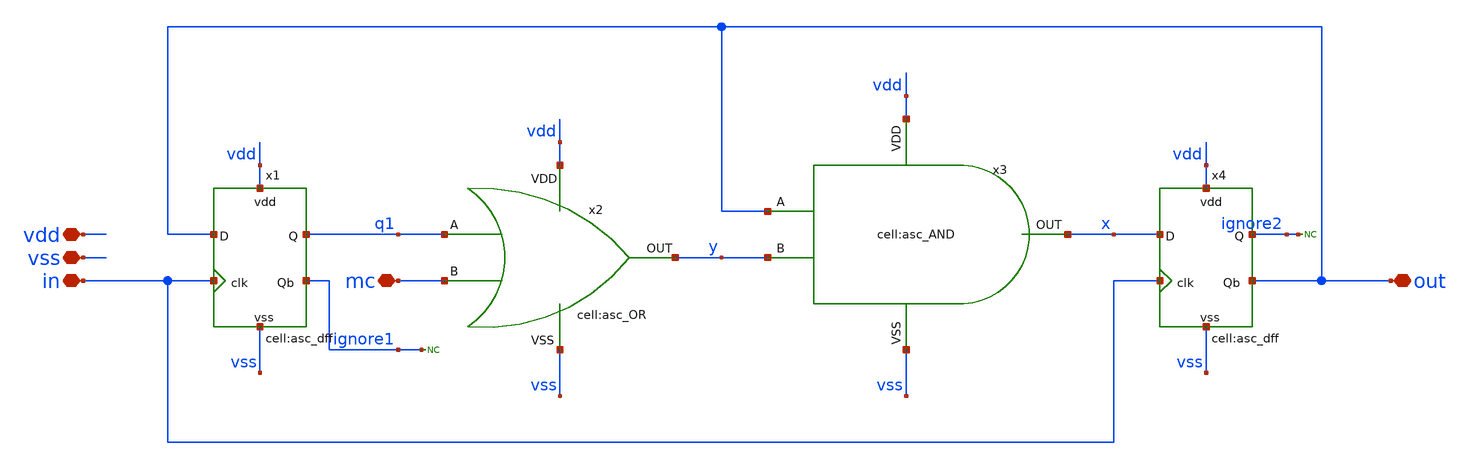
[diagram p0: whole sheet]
** sch_path: designs/libs/core_analog/asc_dual_mod_pre_2_3/asc_dual_mod_pre_2_3.sch
**.subckt asc_dual_mod_pre_2_3 vdd vss in mc out
*.iopin vdd
*.iopin vss
*.iopin in
*.iopin mc
*.iopin out
x1 in out ignore1 vdd vss q1 asc_dff
x2 vdd vss y q1 mc asc_OR
x3 vdd x out y vss asc_AND
x4 in x out vdd vss ignore2 asc_dff
* noconn ignore1
* noconn ignore2
**.ends
.end
